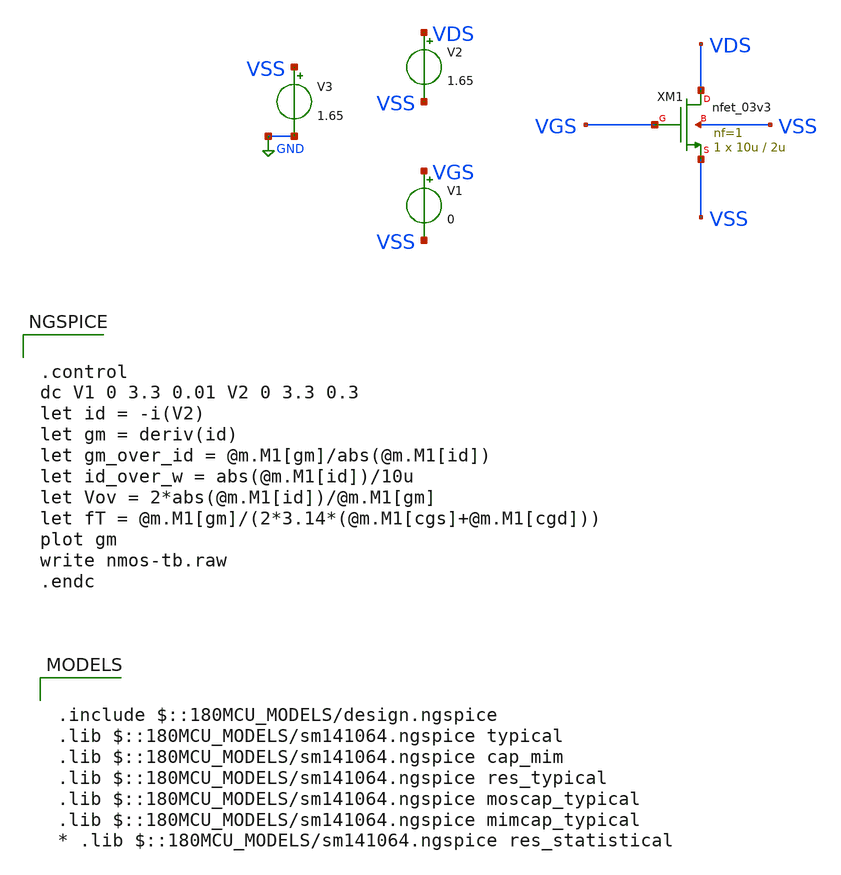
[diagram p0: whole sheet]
** sch_path: w1_advanced-foundation/w1_task/w1_current_mirror/nmos-tb.sch
**.subckt nmos-tb
XM1 VDS VGS VSS VSS nfet_03v3 L=2u W=10u nf=1 ad='int((nf+1)/2) * W/nf * 0.18u' as='int((nf+2)/2) * W/nf * 0.18u'
+ pd='2*int((nf+1)/2) * (W/nf + 0.18u)' ps='2*int((nf+2)/2) * (W/nf + 0.18u)' nrd='0.18u / W' nrs='0.18u / W'
+ sa=0 sb=0 sd=0 m=1
V1 VGS VSS 0
V2 VDS VSS 1.65
V3 VSS net1 1.65
**** begin user architecture code

.include $::180MCU_MODELS/design.ngspice
.lib $::180MCU_MODELS/sm141064.ngspice typical
.lib $::180MCU_MODELS/sm141064.ngspice cap_mim
.lib $::180MCU_MODELS/sm141064.ngspice res_typical
.lib $::180MCU_MODELS/sm141064.ngspice moscap_typical
.lib $::180MCU_MODELS/sm141064.ngspice mimcap_typical
* .lib $::180MCU_MODELS/sm141064.ngspice res_statistical



.control
dc V1 0 3.3 0.01 V2 0 3.3 0.3
let id = -i(V2)
let gm = deriv(id)
let gm_over_id = @m.M1[gm]/abs(@m.M1[id])
let id_over_w = abs(@m.M1[id])/10u
let Vov = 2*abs(@m.M1[id])/@m.M1[gm]
let fT = @m.M1[gm]/(2*3.14*(@m.M1[cgs]+@m.M1[cgd]))
plot gm
write nmos-tb.raw
.endc


**** end user architecture code
**.ends
.GLOBAL GND
.end
